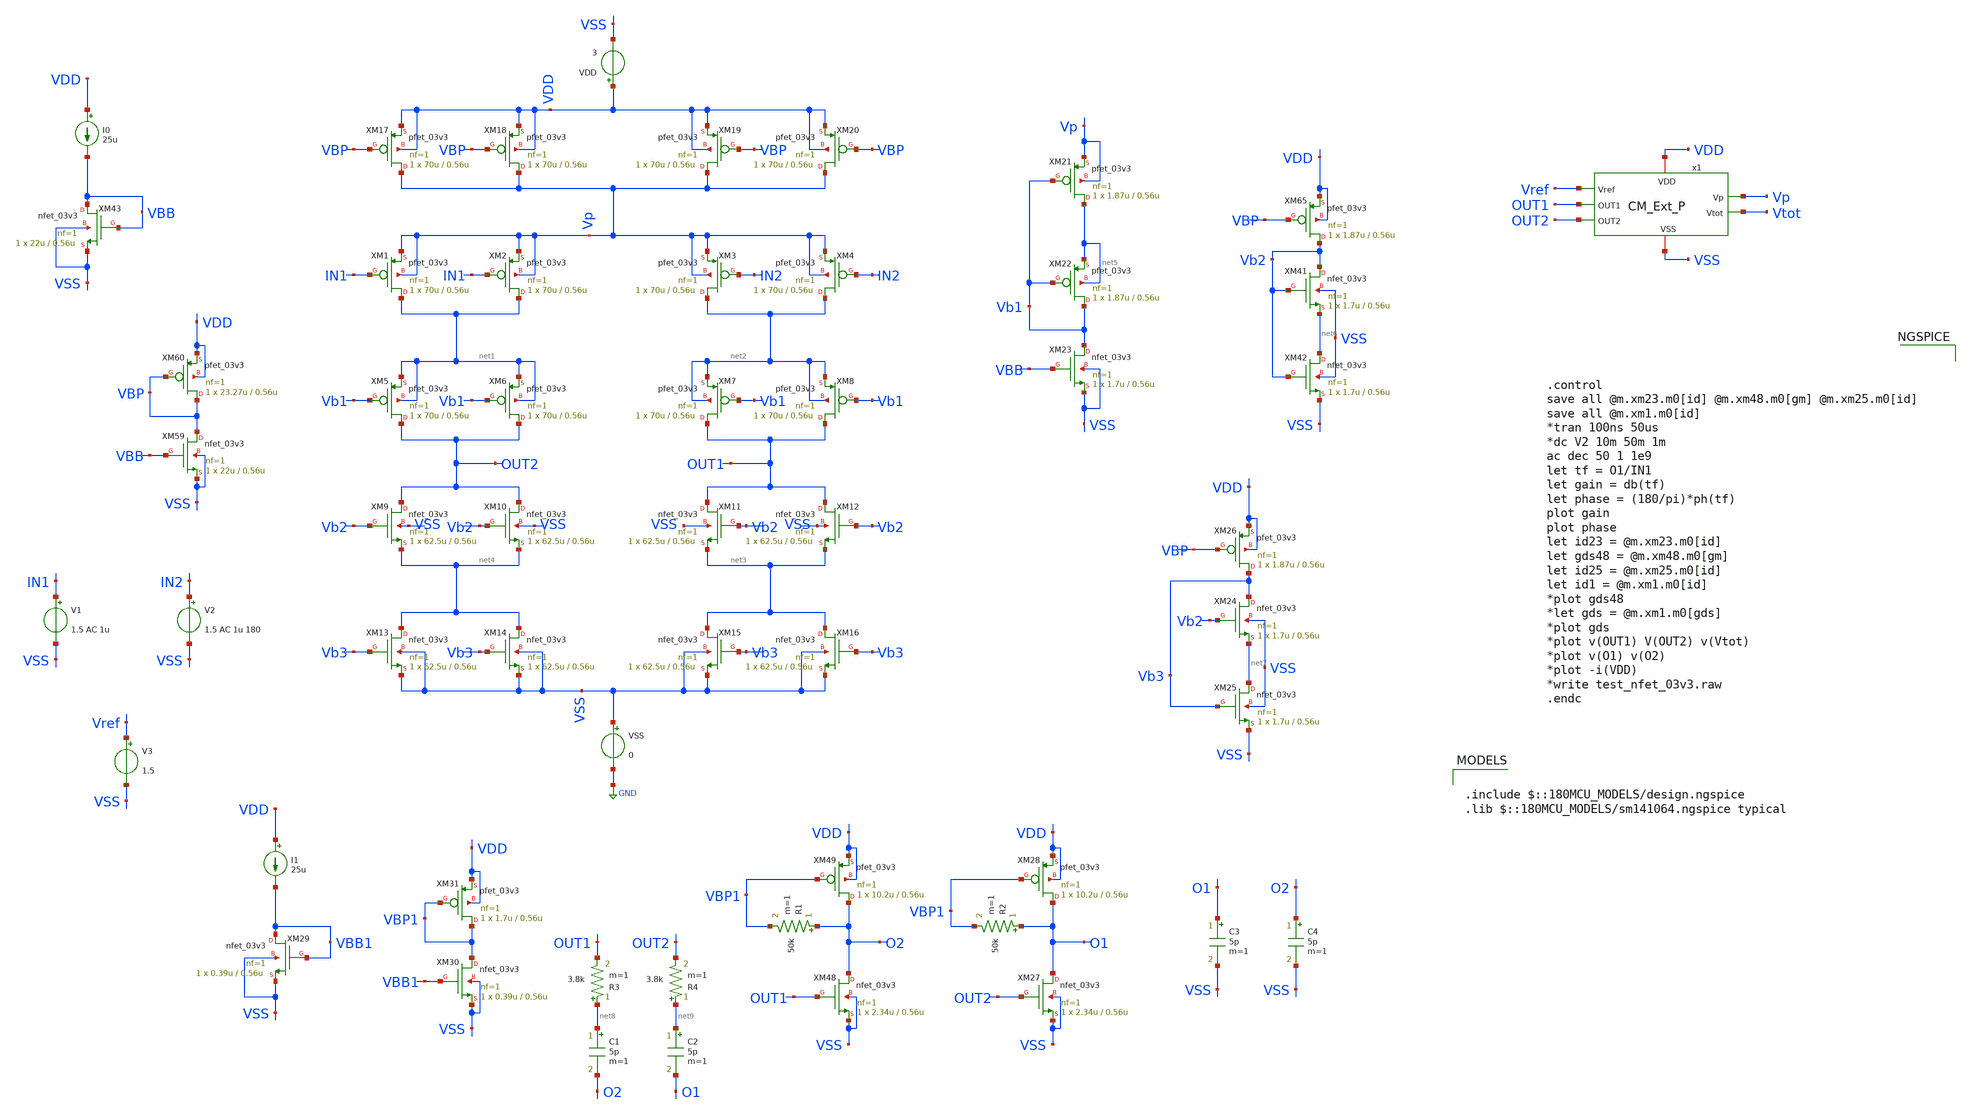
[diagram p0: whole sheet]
** sch_path: SCOP_INPUT_AND_MUX_PAKISTAN_03/Xschem/Others/PMOS_Op_Amp.sch
**.subckt PMOS_Op_Amp
XM1 net1 IN1 Vp Vp pfet_03v3 L=0.56u W=70u nf=1 ad='int((nf+1)/2) * W/nf * 0.18u' as='int((nf+2)/2) * W/nf * 0.18u'
+ pd='2*int((nf+1)/2) * (W/nf + 0.18u)' ps='2*int((nf+2)/2) * (W/nf + 0.18u)' nrd='0.18u / W' nrs='0.18u / W'
+ sa=0 sb=0 sd=0 m=1
XM2 net1 IN1 Vp Vp pfet_03v3 L=0.56u W=70u nf=1 ad='int((nf+1)/2) * W/nf * 0.18u' as='int((nf+2)/2) * W/nf * 0.18u'
+ pd='2*int((nf+1)/2) * (W/nf + 0.18u)' ps='2*int((nf+2)/2) * (W/nf + 0.18u)' nrd='0.18u / W' nrs='0.18u / W'
+ sa=0 sb=0 sd=0 m=1
XM3 net2 IN2 Vp Vp pfet_03v3 L=0.56u W=70u nf=1 ad='int((nf+1)/2) * W/nf * 0.18u' as='int((nf+2)/2) * W/nf * 0.18u'
+ pd='2*int((nf+1)/2) * (W/nf + 0.18u)' ps='2*int((nf+2)/2) * (W/nf + 0.18u)' nrd='0.18u / W' nrs='0.18u / W'
+ sa=0 sb=0 sd=0 m=1
XM4 net2 IN2 Vp Vp pfet_03v3 L=0.56u W=70u nf=1 ad='int((nf+1)/2) * W/nf * 0.18u' as='int((nf+2)/2) * W/nf * 0.18u'
+ pd='2*int((nf+1)/2) * (W/nf + 0.18u)' ps='2*int((nf+2)/2) * (W/nf + 0.18u)' nrd='0.18u / W' nrs='0.18u / W'
+ sa=0 sb=0 sd=0 m=1
XM5 OUT2 Vb1 net1 net1 pfet_03v3 L=0.56u W=70u nf=1 ad='int((nf+1)/2) * W/nf * 0.18u' as='int((nf+2)/2) * W/nf * 0.18u'
+ pd='2*int((nf+1)/2) * (W/nf + 0.18u)' ps='2*int((nf+2)/2) * (W/nf + 0.18u)' nrd='0.18u / W' nrs='0.18u / W'
+ sa=0 sb=0 sd=0 m=1
XM6 OUT2 Vb1 net1 net1 pfet_03v3 L=0.56u W=70u nf=1 ad='int((nf+1)/2) * W/nf * 0.18u' as='int((nf+2)/2) * W/nf * 0.18u'
+ pd='2*int((nf+1)/2) * (W/nf + 0.18u)' ps='2*int((nf+2)/2) * (W/nf + 0.18u)' nrd='0.18u / W' nrs='0.18u / W'
+ sa=0 sb=0 sd=0 m=1
XM7 OUT1 Vb1 net2 net2 pfet_03v3 L=0.56u W=70u nf=1 ad='int((nf+1)/2) * W/nf * 0.18u' as='int((nf+2)/2) * W/nf * 0.18u'
+ pd='2*int((nf+1)/2) * (W/nf + 0.18u)' ps='2*int((nf+2)/2) * (W/nf + 0.18u)' nrd='0.18u / W' nrs='0.18u / W'
+ sa=0 sb=0 sd=0 m=1
XM8 OUT1 Vb1 net2 net2 pfet_03v3 L=0.56u W=70u nf=1 ad='int((nf+1)/2) * W/nf * 0.18u' as='int((nf+2)/2) * W/nf * 0.18u'
+ pd='2*int((nf+1)/2) * (W/nf + 0.18u)' ps='2*int((nf+2)/2) * (W/nf + 0.18u)' nrd='0.18u / W' nrs='0.18u / W'
+ sa=0 sb=0 sd=0 m=1
XM9 OUT2 Vb2 net4 VSS nfet_03v3 L=0.56u W=62.5u nf=1 ad='int((nf+1)/2) * W/nf * 0.18u' as='int((nf+2)/2) * W/nf * 0.18u'
+ pd='2*int((nf+1)/2) * (W/nf + 0.18u)' ps='2*int((nf+2)/2) * (W/nf + 0.18u)' nrd='0.18u / W' nrs='0.18u / W'
+ sa=0 sb=0 sd=0 m=1
XM10 OUT2 Vb2 net4 VSS nfet_03v3 L=0.56u W=62.5u nf=1 ad='int((nf+1)/2) * W/nf * 0.18u' as='int((nf+2)/2) * W/nf * 0.18u'
+ pd='2*int((nf+1)/2) * (W/nf + 0.18u)' ps='2*int((nf+2)/2) * (W/nf + 0.18u)' nrd='0.18u / W' nrs='0.18u / W'
+ sa=0 sb=0 sd=0 m=1
XM11 OUT1 Vb2 net3 VSS nfet_03v3 L=0.56u W=62.5u nf=1 ad='int((nf+1)/2) * W/nf * 0.18u' as='int((nf+2)/2) * W/nf * 0.18u'
+ pd='2*int((nf+1)/2) * (W/nf + 0.18u)' ps='2*int((nf+2)/2) * (W/nf + 0.18u)' nrd='0.18u / W' nrs='0.18u / W'
+ sa=0 sb=0 sd=0 m=1
XM12 OUT1 Vb2 net3 VSS nfet_03v3 L=0.56u W=62.5u nf=1 ad='int((nf+1)/2) * W/nf * 0.18u' as='int((nf+2)/2) * W/nf * 0.18u'
+ pd='2*int((nf+1)/2) * (W/nf + 0.18u)' ps='2*int((nf+2)/2) * (W/nf + 0.18u)' nrd='0.18u / W' nrs='0.18u / W'
+ sa=0 sb=0 sd=0 m=1
XM13 net4 Vb3 VSS VSS nfet_03v3 L=0.56u W=62.5u nf=1 ad='int((nf+1)/2) * W/nf * 0.18u' as='int((nf+2)/2) * W/nf * 0.18u'
+ pd='2*int((nf+1)/2) * (W/nf + 0.18u)' ps='2*int((nf+2)/2) * (W/nf + 0.18u)' nrd='0.18u / W' nrs='0.18u / W'
+ sa=0 sb=0 sd=0 m=1
XM14 net4 Vb3 VSS VSS nfet_03v3 L=0.56u W=62.5u nf=1 ad='int((nf+1)/2) * W/nf * 0.18u' as='int((nf+2)/2) * W/nf * 0.18u'
+ pd='2*int((nf+1)/2) * (W/nf + 0.18u)' ps='2*int((nf+2)/2) * (W/nf + 0.18u)' nrd='0.18u / W' nrs='0.18u / W'
+ sa=0 sb=0 sd=0 m=1
XM15 net3 Vb3 VSS VSS nfet_03v3 L=0.56u W=62.5u nf=1 ad='int((nf+1)/2) * W/nf * 0.18u' as='int((nf+2)/2) * W/nf * 0.18u'
+ pd='2*int((nf+1)/2) * (W/nf + 0.18u)' ps='2*int((nf+2)/2) * (W/nf + 0.18u)' nrd='0.18u / W' nrs='0.18u / W'
+ sa=0 sb=0 sd=0 m=1
XM16 net3 Vb3 VSS VSS nfet_03v3 L=0.56u W=62.5u nf=1 ad='int((nf+1)/2) * W/nf * 0.18u' as='int((nf+2)/2) * W/nf * 0.18u'
+ pd='2*int((nf+1)/2) * (W/nf + 0.18u)' ps='2*int((nf+2)/2) * (W/nf + 0.18u)' nrd='0.18u / W' nrs='0.18u / W'
+ sa=0 sb=0 sd=0 m=1
XM17 Vp VBP VDD VDD pfet_03v3 L=0.56u W=70u nf=1 ad='int((nf+1)/2) * W/nf * 0.18u' as='int((nf+2)/2) * W/nf * 0.18u'
+ pd='2*int((nf+1)/2) * (W/nf + 0.18u)' ps='2*int((nf+2)/2) * (W/nf + 0.18u)' nrd='0.18u / W' nrs='0.18u / W'
+ sa=0 sb=0 sd=0 m=1
XM18 Vp VBP VDD VDD pfet_03v3 L=0.56u W=70u nf=1 ad='int((nf+1)/2) * W/nf * 0.18u' as='int((nf+2)/2) * W/nf * 0.18u'
+ pd='2*int((nf+1)/2) * (W/nf + 0.18u)' ps='2*int((nf+2)/2) * (W/nf + 0.18u)' nrd='0.18u / W' nrs='0.18u / W'
+ sa=0 sb=0 sd=0 m=1
XM19 Vp VBP VDD VDD pfet_03v3 L=0.56u W=70u nf=1 ad='int((nf+1)/2) * W/nf * 0.18u' as='int((nf+2)/2) * W/nf * 0.18u'
+ pd='2*int((nf+1)/2) * (W/nf + 0.18u)' ps='2*int((nf+2)/2) * (W/nf + 0.18u)' nrd='0.18u / W' nrs='0.18u / W'
+ sa=0 sb=0 sd=0 m=1
XM20 Vp VBP VDD VDD pfet_03v3 L=0.56u W=70u nf=1 ad='int((nf+1)/2) * W/nf * 0.18u' as='int((nf+2)/2) * W/nf * 0.18u'
+ pd='2*int((nf+1)/2) * (W/nf + 0.18u)' ps='2*int((nf+2)/2) * (W/nf + 0.18u)' nrd='0.18u / W' nrs='0.18u / W'
+ sa=0 sb=0 sd=0 m=1
XM43 VBB VBB VSS VSS nfet_03v3 L=0.56u W=22u nf=1 ad='int((nf+1)/2) * W/nf * 0.18u' as='int((nf+2)/2) * W/nf * 0.18u'
+ pd='2*int((nf+1)/2) * (W/nf + 0.18u)' ps='2*int((nf+2)/2) * (W/nf + 0.18u)' nrd='0.18u / W' nrs='0.18u / W'
+ sa=0 sb=0 sd=0 m=1
I0 VDD VBB 25u
XM59 VBP VBB VSS VSS nfet_03v3 L=0.56u W=22u nf=1 ad='int((nf+1)/2) * W/nf * 0.18u' as='int((nf+2)/2) * W/nf * 0.18u'
+ pd='2*int((nf+1)/2) * (W/nf + 0.18u)' ps='2*int((nf+2)/2) * (W/nf + 0.18u)' nrd='0.18u / W' nrs='0.18u / W'
+ sa=0 sb=0 sd=0 m=1
XM60 VBP VBP VDD VDD pfet_03v3 L=0.56u W=23.27u nf=1 ad='int((nf+1)/2) * W/nf * 0.18u' as='int((nf+2)/2) * W/nf * 0.18u'
+ pd='2*int((nf+1)/2) * (W/nf + 0.18u)' ps='2*int((nf+2)/2) * (W/nf + 0.18u)' nrd='0.18u / W' nrs='0.18u / W'
+ sa=0 sb=0 sd=0 m=1
XM21 net5 Vb1 Vp Vp pfet_03v3 L=0.56u W=1.87u nf=1 ad='int((nf+1)/2) * W/nf * 0.18u' as='int((nf+2)/2) * W/nf * 0.18u'
+ pd='2*int((nf+1)/2) * (W/nf + 0.18u)' ps='2*int((nf+2)/2) * (W/nf + 0.18u)' nrd='0.18u / W' nrs='0.18u / W'
+ sa=0 sb=0 sd=0 m=1
XM22 Vb1 Vb1 net5 net5 pfet_03v3 L=0.56u W=1.87u nf=1 ad='int((nf+1)/2) * W/nf * 0.18u' as='int((nf+2)/2) * W/nf * 0.18u'
+ pd='2*int((nf+1)/2) * (W/nf + 0.18u)' ps='2*int((nf+2)/2) * (W/nf + 0.18u)' nrd='0.18u / W' nrs='0.18u / W'
+ sa=0 sb=0 sd=0 m=1
XM23 Vb1 VBB VSS VSS nfet_03v3 L=0.56u W=1.7u nf=1 ad='int((nf+1)/2) * W/nf * 0.18u' as='int((nf+2)/2) * W/nf * 0.18u'
+ pd='2*int((nf+1)/2) * (W/nf + 0.18u)' ps='2*int((nf+2)/2) * (W/nf + 0.18u)' nrd='0.18u / W' nrs='0.18u / W'
+ sa=0 sb=0 sd=0 m=1
XM41 Vb2 Vb2 net6 VSS nfet_03v3 L=0.56u W=1.7u nf=1 ad='int((nf+1)/2) * W/nf * 0.18u' as='int((nf+2)/2) * W/nf * 0.18u'
+ pd='2*int((nf+1)/2) * (W/nf + 0.18u)' ps='2*int((nf+2)/2) * (W/nf + 0.18u)' nrd='0.18u / W' nrs='0.18u / W'
+ sa=0 sb=0 sd=0 m=1
XM42 net6 Vb2 VSS VSS nfet_03v3 L=0.56u W=1.7u nf=1 ad='int((nf+1)/2) * W/nf * 0.18u' as='int((nf+2)/2) * W/nf * 0.18u'
+ pd='2*int((nf+1)/2) * (W/nf + 0.18u)' ps='2*int((nf+2)/2) * (W/nf + 0.18u)' nrd='0.18u / W' nrs='0.18u / W'
+ sa=0 sb=0 sd=0 m=1
XM65 Vb2 VBP VDD VDD pfet_03v3 L=0.56u W=1.87u nf=1 ad='int((nf+1)/2) * W/nf * 0.18u' as='int((nf+2)/2) * W/nf * 0.18u'
+ pd='2*int((nf+1)/2) * (W/nf + 0.18u)' ps='2*int((nf+2)/2) * (W/nf + 0.18u)' nrd='0.18u / W' nrs='0.18u / W'
+ sa=0 sb=0 sd=0 m=1
XM24 Vb3 Vb2 net7 VSS nfet_03v3 L=0.56u W=1.7u nf=1 ad='int((nf+1)/2) * W/nf * 0.18u' as='int((nf+2)/2) * W/nf * 0.18u'
+ pd='2*int((nf+1)/2) * (W/nf + 0.18u)' ps='2*int((nf+2)/2) * (W/nf + 0.18u)' nrd='0.18u / W' nrs='0.18u / W'
+ sa=0 sb=0 sd=0 m=1
XM25 net7 Vb3 VSS VSS nfet_03v3 L=0.56u W=1.7u nf=1 ad='int((nf+1)/2) * W/nf * 0.18u' as='int((nf+2)/2) * W/nf * 0.18u'
+ pd='2*int((nf+1)/2) * (W/nf + 0.18u)' ps='2*int((nf+2)/2) * (W/nf + 0.18u)' nrd='0.18u / W' nrs='0.18u / W'
+ sa=0 sb=0 sd=0 m=1
XM26 Vb3 VBP VDD VDD pfet_03v3 L=0.56u W=1.87u nf=1 ad='int((nf+1)/2) * W/nf * 0.18u' as='int((nf+2)/2) * W/nf * 0.18u'
+ pd='2*int((nf+1)/2) * (W/nf + 0.18u)' ps='2*int((nf+2)/2) * (W/nf + 0.18u)' nrd='0.18u / W' nrs='0.18u / W'
+ sa=0 sb=0 sd=0 m=1
V1 IN1 VSS 1.5 AC 1u
V2 IN2 VSS 1.5 AC 1u 180
VSS VSS GND 0
VDD VDD VSS 3
x1 Vref Vp Vtot VDD OUT1 VSS OUT2 CM_Ext_P
V3 Vref VSS 1.5
XM48 O2 OUT1 VSS VSS nfet_03v3 L=0.56u W=2.34u nf=1 ad='int((nf+1)/2) * W/nf * 0.18u' as='int((nf+2)/2) * W/nf * 0.18u'
+ pd='2*int((nf+1)/2) * (W/nf + 0.18u)' ps='2*int((nf+2)/2) * (W/nf + 0.18u)' nrd='0.18u / W' nrs='0.18u / W'
+ sa=0 sb=0 sd=0 m=1
XM49 O2 VBP1 VDD VDD pfet_03v3 L=0.56u W=10.2u nf=1 ad='int((nf+1)/2) * W/nf * 0.18u' as='int((nf+2)/2) * W/nf * 0.18u'
+ pd='2*int((nf+1)/2) * (W/nf + 0.18u)' ps='2*int((nf+2)/2) * (W/nf + 0.18u)' nrd='0.18u / W' nrs='0.18u / W'
+ sa=0 sb=0 sd=0 m=1
XM27 O1 OUT2 VSS VSS nfet_03v3 L=0.56u W=2.34u nf=1 ad='int((nf+1)/2) * W/nf * 0.18u' as='int((nf+2)/2) * W/nf * 0.18u'
+ pd='2*int((nf+1)/2) * (W/nf + 0.18u)' ps='2*int((nf+2)/2) * (W/nf + 0.18u)' nrd='0.18u / W' nrs='0.18u / W'
+ sa=0 sb=0 sd=0 m=1
XM28 O1 VBP1 VDD VDD pfet_03v3 L=0.56u W=10.2u nf=1 ad='int((nf+1)/2) * W/nf * 0.18u' as='int((nf+2)/2) * W/nf * 0.18u'
+ pd='2*int((nf+1)/2) * (W/nf + 0.18u)' ps='2*int((nf+2)/2) * (W/nf + 0.18u)' nrd='0.18u / W' nrs='0.18u / W'
+ sa=0 sb=0 sd=0 m=1
XM29 VBB1 VBB1 VSS VSS nfet_03v3 L=0.56u W=0.39u nf=1 ad='int((nf+1)/2) * W/nf * 0.18u' as='int((nf+2)/2) * W/nf * 0.18u'
+ pd='2*int((nf+1)/2) * (W/nf + 0.18u)' ps='2*int((nf+2)/2) * (W/nf + 0.18u)' nrd='0.18u / W' nrs='0.18u / W'
+ sa=0 sb=0 sd=0 m=1
I1 VDD VBB1 25u
XM30 VBP1 VBB1 VSS VSS nfet_03v3 L=0.56u W=0.39u nf=1 ad='int((nf+1)/2) * W/nf * 0.18u' as='int((nf+2)/2) * W/nf * 0.18u'
+ pd='2*int((nf+1)/2) * (W/nf + 0.18u)' ps='2*int((nf+2)/2) * (W/nf + 0.18u)' nrd='0.18u / W' nrs='0.18u / W'
+ sa=0 sb=0 sd=0 m=1
XM31 VBP1 VBP1 VDD VDD pfet_03v3 L=0.56u W=1.7u nf=1 ad='int((nf+1)/2) * W/nf * 0.18u' as='int((nf+2)/2) * W/nf * 0.18u'
+ pd='2*int((nf+1)/2) * (W/nf + 0.18u)' ps='2*int((nf+2)/2) * (W/nf + 0.18u)' nrd='0.18u / W' nrs='0.18u / W'
+ sa=0 sb=0 sd=0 m=1
R1 O2 VBP1 50k m=1
R2 O1 VBP1 50k m=1
C1 net8 O2 5p m=1
C2 net9 O1 5p m=1
R3 net8 OUT1 3.8k m=1
R4 net9 OUT2 3.8k m=1
C3 O1 VSS 5p m=1
C4 O2 VSS 5p m=1
**** begin user architecture code

.include $::180MCU_MODELS/design.ngspice
.lib $::180MCU_MODELS/sm141064.ngspice typical




.control
save all @m.xm23.m0[id] @m.xm48.m0[gm] @m.xm25.m0[id]
save all @m.xm1.m0[id]
*tran 100ns 50us
*dc V2 10m 50m 1m
ac dec 50 1 1e9
let tf = O1/IN1
let gain = db(tf)
let phase = (180/pi)*ph(tf)
plot gain
plot phase
let id23 = @m.xm23.m0[id]
let gds48 = @m.xm48.m0[gm]
let id25 = @m.xm25.m0[id]
let id1 = @m.xm1.m0[id]
*plot gds48
*let gds = @m.xm1.m0[gds]
*plot gds
*plot v(OUT1) V(OUT2) v(Vtot)
*plot v(O1) v(O2)
*plot -i(VDD)
*write test_nfet_03v3.raw
.endc


**** end user architecture code
**.ends

* expanding   symbol:  Tapeout/CM_Ext_P.sym # of pins=7
** sym_path: SCOP_INPUT_AND_MUX_PAKISTAN_03/Xschem/Others/CM_Ext_P.sym
** sch_path: SCOP_INPUT_AND_MUX_PAKISTAN_03/Xschem/Others/CM_Ext_P.sch
.subckt CM_Ext_P Vref Vp Vtot VDD OUT1 VSS OUT2
*.ipin Vref
*.ipin OUT1
*.ipin OUT2
*.opin Vp
*.iopin VDD
*.iopin VSS
*.opin Vtot
R2 Vtot VB 100k m=1
R1 Vtot VA 100k m=1
R4 VD Vtot 100k m=1
R3 VC Vtot 100k m=1
XM50 VSS OUT2 VC VC pfet_03v3 L=0.56u W=9.35u nf=1 ad='int((nf+1)/2) * W/nf * 0.18u' as='int((nf+2)/2) * W/nf * 0.18u'
+ pd='2*int((nf+1)/2) * (W/nf + 0.18u)' ps='2*int((nf+2)/2) * (W/nf + 0.18u)' nrd='0.18u / W' nrs='0.18u / W'
+ sa=0 sb=0 sd=0 m=1
XM51 VSS OUT1 VD VD pfet_03v3 L=0.56u W=9.35u nf=1 ad='int((nf+1)/2) * W/nf * 0.18u' as='int((nf+2)/2) * W/nf * 0.18u'
+ pd='2*int((nf+1)/2) * (W/nf + 0.18u)' ps='2*int((nf+2)/2) * (W/nf + 0.18u)' nrd='0.18u / W' nrs='0.18u / W'
+ sa=0 sb=0 sd=0 m=1
XM61 VD VBP VDD VDD pfet_03v3 L=0.56u W=9.35u nf=1 ad='int((nf+1)/2) * W/nf * 0.18u' as='int((nf+2)/2) * W/nf * 0.18u'
+ pd='2*int((nf+1)/2) * (W/nf + 0.18u)' ps='2*int((nf+2)/2) * (W/nf + 0.18u)' nrd='0.18u / W' nrs='0.18u / W'
+ sa=0 sb=0 sd=0 m=1
XM62 VC VBP VDD VDD pfet_03v3 L=0.56u W=9.35u nf=1 ad='int((nf+1)/2) * W/nf * 0.18u' as='int((nf+2)/2) * W/nf * 0.18u'
+ pd='2*int((nf+1)/2) * (W/nf + 0.18u)' ps='2*int((nf+2)/2) * (W/nf + 0.18u)' nrd='0.18u / W' nrs='0.18u / W'
+ sa=0 sb=0 sd=0 m=1
XM59 VBP VBB VSS VSS nfet_03v3 L=0.56u W=8.8u nf=1 ad='int((nf+1)/2) * W/nf * 0.18u' as='int((nf+2)/2) * W/nf * 0.18u'
+ pd='2*int((nf+1)/2) * (W/nf + 0.18u)' ps='2*int((nf+2)/2) * (W/nf + 0.18u)' nrd='0.18u / W' nrs='0.18u / W'
+ sa=0 sb=0 sd=0 m=1
XM60 VBP VBP VDD VDD pfet_03v3 L=0.56u W=9.35u nf=1 ad='int((nf+1)/2) * W/nf * 0.18u' as='int((nf+2)/2) * W/nf * 0.18u'
+ pd='2*int((nf+1)/2) * (W/nf + 0.18u)' ps='2*int((nf+2)/2) * (W/nf + 0.18u)' nrd='0.18u / W' nrs='0.18u / W'
+ sa=0 sb=0 sd=0 m=1
XM49 VDD OUT1 VB VSS nfet_03v3 L=0.56u W=8.8u nf=1 ad='int((nf+1)/2) * W/nf * 0.18u' as='int((nf+2)/2) * W/nf * 0.18u'
+ pd='2*int((nf+1)/2) * (W/nf + 0.18u)' ps='2*int((nf+2)/2) * (W/nf + 0.18u)' nrd='0.18u / W' nrs='0.18u / W'
+ sa=0 sb=0 sd=0 m=1
XM58 VB VBB VSS VSS nfet_03v3 L=0.56u W=8.8u nf=1 ad='int((nf+1)/2) * W/nf * 0.18u' as='int((nf+2)/2) * W/nf * 0.18u'
+ pd='2*int((nf+1)/2) * (W/nf + 0.18u)' ps='2*int((nf+2)/2) * (W/nf + 0.18u)' nrd='0.18u / W' nrs='0.18u / W'
+ sa=0 sb=0 sd=0 m=1
XM48 VDD OUT2 VA VSS nfet_03v3 L=0.56u W=8.8u nf=1 ad='int((nf+1)/2) * W/nf * 0.18u' as='int((nf+2)/2) * W/nf * 0.18u'
+ pd='2*int((nf+1)/2) * (W/nf + 0.18u)' ps='2*int((nf+2)/2) * (W/nf + 0.18u)' nrd='0.18u / W' nrs='0.18u / W'
+ sa=0 sb=0 sd=0 m=1
XM57 VA VBB VSS VSS nfet_03v3 L=0.56u W=8.8u nf=1 ad='int((nf+1)/2) * W/nf * 0.18u' as='int((nf+2)/2) * W/nf * 0.18u'
+ pd='2*int((nf+1)/2) * (W/nf + 0.18u)' ps='2*int((nf+2)/2) * (W/nf + 0.18u)' nrd='0.18u / W' nrs='0.18u / W'
+ sa=0 sb=0 sd=0 m=1
XM43 VBB VBB VSS VSS nfet_03v3 L=0.56u W=22u nf=1 ad='int((nf+1)/2) * W/nf * 0.18u' as='int((nf+2)/2) * W/nf * 0.18u'
+ pd='2*int((nf+1)/2) * (W/nf + 0.18u)' ps='2*int((nf+2)/2) * (W/nf + 0.18u)' nrd='0.18u / W' nrs='0.18u / W'
+ sa=0 sb=0 sd=0 m=1
I0 VDD VBB 25u
XM1 net1 net1 VDD VDD pfet_03v3 L=0.56u W=23.4u nf=1 ad='int((nf+1)/2) * W/nf * 0.18u' as='int((nf+2)/2) * W/nf * 0.18u'
+ pd='2*int((nf+1)/2) * (W/nf + 0.18u)' ps='2*int((nf+2)/2) * (W/nf + 0.18u)' nrd='0.18u / W' nrs='0.18u / W'
+ sa=0 sb=0 sd=0 m=1
XM2 net2 net1 VDD VDD pfet_03v3 L=0.56u W=23.4u nf=1 ad='int((nf+1)/2) * W/nf * 0.18u' as='int((nf+2)/2) * W/nf * 0.18u'
+ pd='2*int((nf+1)/2) * (W/nf + 0.18u)' ps='2*int((nf+2)/2) * (W/nf + 0.18u)' nrd='0.18u / W' nrs='0.18u / W'
+ sa=0 sb=0 sd=0 m=1
XM3 net1 Vtot net3 VSS nfet_03v3 L=0.56u W=22u nf=1 ad='int((nf+1)/2) * W/nf * 0.18u' as='int((nf+2)/2) * W/nf * 0.18u'
+ pd='2*int((nf+1)/2) * (W/nf + 0.18u)' ps='2*int((nf+2)/2) * (W/nf + 0.18u)' nrd='0.18u / W' nrs='0.18u / W'
+ sa=0 sb=0 sd=0 m=1
XM4 net2 Vref net3 VSS nfet_03v3 L=0.56u W=22u nf=1 ad='int((nf+1)/2) * W/nf * 0.18u' as='int((nf+2)/2) * W/nf * 0.18u'
+ pd='2*int((nf+1)/2) * (W/nf + 0.18u)' ps='2*int((nf+2)/2) * (W/nf + 0.18u)' nrd='0.18u / W' nrs='0.18u / W'
+ sa=0 sb=0 sd=0 m=1
XM5 net3 VBB VSS VSS nfet_03v3 L=0.56u W=22u nf=1 ad='int((nf+1)/2) * W/nf * 0.18u' as='int((nf+2)/2) * W/nf * 0.18u'
+ pd='2*int((nf+1)/2) * (W/nf + 0.18u)' ps='2*int((nf+2)/2) * (W/nf + 0.18u)' nrd='0.18u / W' nrs='0.18u / W'
+ sa=0 sb=0 sd=0 m=1
XM6 Vp net2 VDD VDD pfet_03v3 L=0.56u W=23.4u nf=1 ad='int((nf+1)/2) * W/nf * 0.18u' as='int((nf+2)/2) * W/nf * 0.18u'
+ pd='2*int((nf+1)/2) * (W/nf + 0.18u)' ps='2*int((nf+2)/2) * (W/nf + 0.18u)' nrd='0.18u / W' nrs='0.18u / W'
+ sa=0 sb=0 sd=0 m=1
.ends

.GLOBAL GND
.end
